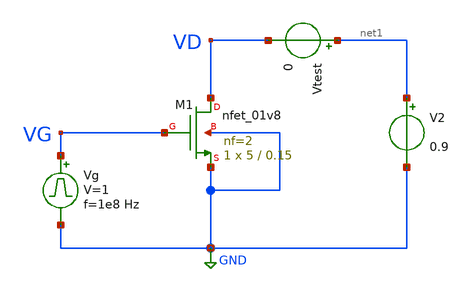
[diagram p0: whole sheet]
** sch_path: design/bgr/test2.sch
**.subckt test2
V2 net1 GND 0.9
XM1 VD VG GND GND sky130_fd_pr__nfet_01v8 L=0.15 W=5 nf=2 ad='int((nf+1)/2) * W/nf * 0.29' as='int((nf+2)/2) * W/nf * 0.29'
+ pd='2*int((nf+1)/2) * (W/nf + 0.29)' ps='2*int((nf+2)/2) * (W/nf + 0.29)' nrd='0.29 / W' nrs='0.29 / W'
+ sa=0 sb=0 sd=0 mult=1 m=1
Vg VG GND pulse 0 1 '0.495/ 1e8 ' '0.01/1e8 ' '0.01/1e8 ' '0.49/1e8 ' '1/1e8 '
Vtest net1 VD 0
**** begin user architecture code


.param temp=27

*.op
*.ac dec 10 1 10G


.control
tran 1n 500n 200n
save all
options savecurrents
save all @m.xm1.msky130_fd_pr__nfet_01v8[id] @m.xm1.msky130_fd_pr__nfet_01v8[gm]
plot VG
plot i(Vtest)

*plot i(V2)
.endc

.save all





.options wnflag=1
.include $::SKYWATER_MODELS/cells/nfet_01v8/sky130_fd_pr__nfet_01v8__tt.corner.spice
.include $::SKYWATER_MODELS/cells/nfet_01v8_lvt/sky130_fd_pr__nfet_01v8_lvt__tt.corner.spice
.include $::SKYWATER_MODELS/cells/pfet_01v8/sky130_fd_pr__pfet_01v8__tt.corner.spice
.include $::SKYWATER_MODELS/cells/nfet_03v3_nvt/sky130_fd_pr__nfet_03v3_nvt__tt.corner.spice
.include $::SKYWATER_MODELS/cells/nfet_05v0_nvt/sky130_fd_pr__nfet_05v0_nvt__tt.corner.spice
.include $::SKYWATER_MODELS/cells/esd_nfet_01v8/sky130_fd_pr__esd_nfet_01v8__tt.corner.spice
.include $::SKYWATER_MODELS/cells/pfet_01v8_lvt/sky130_fd_pr__pfet_01v8_lvt__tt.corner.spice
.include $::SKYWATER_MODELS/cells/pfet_01v8_hvt/sky130_fd_pr__pfet_01v8_hvt__tt.corner.spice
.include $::SKYWATER_MODELS/cells/esd_pfet_g5v0d10v5/sky130_fd_pr__esd_pfet_g5v0d10v5__tt.corner.spice
.include $::SKYWATER_MODELS/cells/pfet_g5v0d10v5/sky130_fd_pr__pfet_g5v0d10v5__tt.corner.spice
.include $::SKYWATER_MODELS/cells/pfet_g5v0d16v0/sky130_fd_pr__pfet_g5v0d16v0__tt.corner.spice
.include $::SKYWATER_MODELS/cells/nfet_g5v0d10v5/sky130_fd_pr__nfet_g5v0d10v5__tt.corner.spice
.include $::SKYWATER_MODELS/cells/nfet_g5v0d16v0/sky130_fd_pr__nfet_g5v0d16v0__tt_discrete.corner.spice
.include $::SKYWATER_MODELS/cells/esd_nfet_g5v0d10v5/sky130_fd_pr__esd_nfet_g5v0d10v5__tt.corner.spice
.include $::SKYWATER_MODELS/models/corners/tt/nonfet.spice
* Mismatch parameters
.include $::SKYWATER_MODELS/cells/nfet_01v8/sky130_fd_pr__nfet_01v8__mismatch.corner.spice
.include $::SKYWATER_MODELS/cells/pfet_01v8/sky130_fd_pr__pfet_01v8__mismatch.corner.spice
.include $::SKYWATER_MODELS/cells/nfet_01v8_lvt/sky130_fd_pr__nfet_01v8_lvt__mismatch.corner.spice
.include $::SKYWATER_MODELS/cells/pfet_01v8_lvt/sky130_fd_pr__pfet_01v8_lvt__mismatch.corner.spice
.include $::SKYWATER_MODELS/cells/pfet_01v8_hvt/sky130_fd_pr__pfet_01v8_hvt__mismatch.corner.spice
.include $::SKYWATER_MODELS/cells/nfet_g5v0d10v5/sky130_fd_pr__nfet_g5v0d10v5__mismatch.corner.spice
.include $::SKYWATER_MODELS/cells/pfet_g5v0d10v5/sky130_fd_pr__pfet_g5v0d10v5__mismatch.corner.spice
.include $::SKYWATER_MODELS/cells/nfet_05v0_nvt/sky130_fd_pr__nfet_05v0_nvt__mismatch.corner.spice
.include $::SKYWATER_MODELS/cells/nfet_03v3_nvt/sky130_fd_pr__nfet_03v3_nvt__mismatch.corner.spice
* Resistor$::SKYWATER_MODELS/Capacitor
.include $::SKYWATER_MODELS/models/r+c/res_typical__cap_typical.spice
.include $::SKYWATER_MODELS/models/r+c/res_typical__cap_typical__lin.spice
* Special cells
.include $::SKYWATER_MODELS/models/corners/tt/specialized_cells.spice
* All models
.include $::SKYWATER_MODELS/models/all.spice
* Corner
.include $::SKYWATER_MODELS/models/corners/tt/rf.spice

**** end user architecture code
**.ends
.GLOBAL GND
.end
